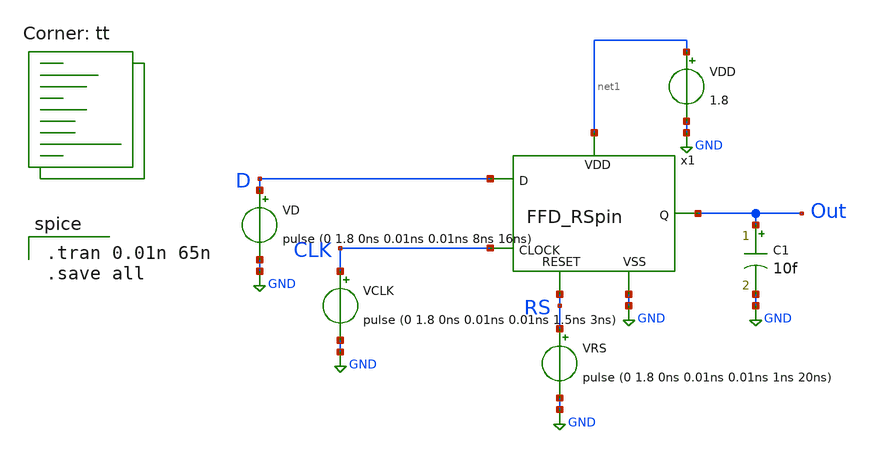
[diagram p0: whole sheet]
** sch_path: FFD_RSpin_tb.sch
**.subckt FFD_RSpin_tb
VD D GND pulse (0 1.8 0ns 0.01ns 0.01ns 8ns 16ns)
VCLK CLK GND pulse (0 1.8 0ns 0.01ns 0.01ns 1.5ns 3ns)
VRS RS GND pulse (0 1.8 0ns 0.01ns 0.01ns 1ns 20ns)
VDD net1 GND 1.8
x1 net1 GND RS CLK Out D FFD_RSpin
C1 Out GND 10f m=1
**** begin user architecture code
.lib $::SKYWATER_MODELS/sky130.lib.spice tt

.tran 0.01n 65n
.save all

**** end user architecture code
**.ends

* expanding   symbol:  project/FFD_RSpin.sym # of pins=6
** sym_path: FFD_RSpin.sym
** sch_path: FFD_RSpin.sch
.subckt FFD_RSpin VDD VSS RESET CLOCK Q D
*.ipin CLOCK
*.ipin D
*.ipin RESET
*.ipin VDD
*.ipin VSS
*.opin Q
XM1 D CLKB net1 VSS sky130_fd_pr__nfet_01v8 L=0.15 W=0.5 nf=1 ad='int((nf+1)/2) * W/nf * 0.29' as='int((nf+2)/2) * W/nf * 0.29'
+ pd='2*int((nf+1)/2) * (W/nf + 0.29)' ps='2*int((nf+2)/2) * (W/nf + 0.29)' nrd='0.29 / W' nrs='0.29 / W'
+ sa=0 sb=0 sd=0 mult=1 m=1
XM2 D CLK net1 VDD sky130_fd_pr__pfet_01v8 L=0.15 W=1 nf=1 ad='int((nf+1)/2) * W/nf * 0.29' as='int((nf+2)/2) * W/nf * 0.29'
+ pd='2*int((nf+1)/2) * (W/nf + 0.29)' ps='2*int((nf+2)/2) * (W/nf + 0.29)' nrd='0.29 / W' nrs='0.29 / W'
+ sa=0 sb=0 sd=0 mult=1 m=1
XM3 net2 CLK net3 VSS sky130_fd_pr__nfet_01v8 L=0.15 W=0.5 nf=1 ad='int((nf+1)/2) * W/nf * 0.29' as='int((nf+2)/2) * W/nf * 0.29'
+ pd='2*int((nf+1)/2) * (W/nf + 0.29)' ps='2*int((nf+2)/2) * (W/nf + 0.29)' nrd='0.29 / W' nrs='0.29 / W'
+ sa=0 sb=0 sd=0 mult=1 m=1
XM4 net2 CLKB net3 VDD sky130_fd_pr__pfet_01v8 L=0.15 W=1 nf=1 ad='int((nf+1)/2) * W/nf * 0.29' as='int((nf+2)/2) * W/nf * 0.29'
+ pd='2*int((nf+1)/2) * (W/nf + 0.29)' ps='2*int((nf+2)/2) * (W/nf + 0.29)' nrd='0.29 / W' nrs='0.29 / W'
+ sa=0 sb=0 sd=0 mult=1 m=1
XM5 net1 CLK net5 VSS sky130_fd_pr__nfet_01v8 L=0.15 W=0.5 nf=1 ad='int((nf+1)/2) * W/nf * 0.29' as='int((nf+2)/2) * W/nf * 0.29'
+ pd='2*int((nf+1)/2) * (W/nf + 0.29)' ps='2*int((nf+2)/2) * (W/nf + 0.29)' nrd='0.29 / W' nrs='0.29 / W'
+ sa=0 sb=0 sd=0 mult=1 m=1
XM6 net1 CLKB net5 VDD sky130_fd_pr__pfet_01v8 L=0.15 W=1 nf=1 ad='int((nf+1)/2) * W/nf * 0.29' as='int((nf+2)/2) * W/nf * 0.29'
+ pd='2*int((nf+1)/2) * (W/nf + 0.29)' ps='2*int((nf+2)/2) * (W/nf + 0.29)' nrd='0.29 / W' nrs='0.29 / W'
+ sa=0 sb=0 sd=0 mult=1 m=1
XM7 net3 CLKB net6 VSS sky130_fd_pr__nfet_01v8 L=0.15 W=0.5 nf=1 ad='int((nf+1)/2) * W/nf * 0.29' as='int((nf+2)/2) * W/nf * 0.29'
+ pd='2*int((nf+1)/2) * (W/nf + 0.29)' ps='2*int((nf+2)/2) * (W/nf + 0.29)' nrd='0.29 / W' nrs='0.29 / W'
+ sa=0 sb=0 sd=0 mult=1 m=1
XM8 net3 CLK net6 VDD sky130_fd_pr__pfet_01v8 L=0.15 W=1 nf=1 ad='int((nf+1)/2) * W/nf * 0.29' as='int((nf+2)/2) * W/nf * 0.29'
+ pd='2*int((nf+1)/2) * (W/nf + 0.29)' ps='2*int((nf+2)/2) * (W/nf + 0.29)' nrd='0.29 / W' nrs='0.29 / W'
+ sa=0 sb=0 sd=0 mult=1 m=1
x2 VDD RESET net3 net4 VSS nor_FFD
x3 VDD RESET net1 net2 VSS nor_FFD
x7 VDD CLOCK CLKB VSS Inverter
x8 VDD CLKB CLK VSS Inverter
x1 VDD net4 net7 VSS Inverter
x4 VDD net7 Q VSS Inverter
x5 VDD net2 net5 VSS Inverter
x6 VDD net4 net6 VSS Inverter
.ends


* expanding   symbol:  nor_FFD.sym # of pins=5
** sym_path: nor_FFD.sym
** sch_path: nor_FFD.sch
.subckt nor_FFD VDD A B Y VSS
*.ipin VDD
*.ipin A
*.ipin B
*.ipin VSS
*.opin Y
XM1 Y A VSS VSS sky130_fd_pr__nfet_01v8 L=0.15 W=0.5 nf=1 ad='int((nf+1)/2) * W/nf * 0.29' as='int((nf+2)/2) * W/nf * 0.29'
+ pd='2*int((nf+1)/2) * (W/nf + 0.29)' ps='2*int((nf+2)/2) * (W/nf + 0.29)' nrd='0.29 / W' nrs='0.29 / W'
+ sa=0 sb=0 sd=0 mult=1 m=1
XM2 Y B VSS VSS sky130_fd_pr__nfet_01v8 L=0.15 W=0.5 nf=1 ad='int((nf+1)/2) * W/nf * 0.29' as='int((nf+2)/2) * W/nf * 0.29'
+ pd='2*int((nf+1)/2) * (W/nf + 0.29)' ps='2*int((nf+2)/2) * (W/nf + 0.29)' nrd='0.29 / W' nrs='0.29 / W'
+ sa=0 sb=0 sd=0 mult=1 m=1
XM3 net1 A VDD VDD sky130_fd_pr__pfet_01v8 L=0.15 W=2.5 nf=1 ad='int((nf+1)/2) * W/nf * 0.29' as='int((nf+2)/2) * W/nf * 0.29'
+ pd='2*int((nf+1)/2) * (W/nf + 0.29)' ps='2*int((nf+2)/2) * (W/nf + 0.29)' nrd='0.29 / W' nrs='0.29 / W'
+ sa=0 sb=0 sd=0 mult=1 m=1
XM4 Y B net1 VDD sky130_fd_pr__pfet_01v8 L=0.15 W=2.5 nf=1 ad='int((nf+1)/2) * W/nf * 0.29' as='int((nf+2)/2) * W/nf * 0.29'
+ pd='2*int((nf+1)/2) * (W/nf + 0.29)' ps='2*int((nf+2)/2) * (W/nf + 0.29)' nrd='0.29 / W' nrs='0.29 / W'
+ sa=0 sb=0 sd=0 mult=1 m=1
.ends


* expanding   symbol:  Inverter.sym # of pins=4
** sym_path: Inverter.sym
** sch_path: Inverter.sch
.subckt Inverter VDD IN OUT VSS
*.ipin IN
*.ipin VSS
*.ipin VDD
*.opin OUT
XM1 OUT IN VSS VSS sky130_fd_pr__nfet_01v8 L=0.3 W=1 nf=1 ad='int((nf+1)/2) * W/nf * 0.29' as='int((nf+2)/2) * W/nf * 0.29'
+ pd='2*int((nf+1)/2) * (W/nf + 0.29)' ps='2*int((nf+2)/2) * (W/nf + 0.29)' nrd='0.29 / W' nrs='0.29 / W'
+ sa=0 sb=0 sd=0 mult=1 m=1
XM2 OUT IN VDD VDD sky130_fd_pr__pfet_01v8 L=0.3 W=2 nf=1 ad='int((nf+1)/2) * W/nf * 0.29' as='int((nf+2)/2) * W/nf * 0.29'
+ pd='2*int((nf+1)/2) * (W/nf + 0.29)' ps='2*int((nf+2)/2) * (W/nf + 0.29)' nrd='0.29 / W' nrs='0.29 / W'
+ sa=0 sb=0 sd=0 mult=1 m=1
.ends

.GLOBAL GND
.end
